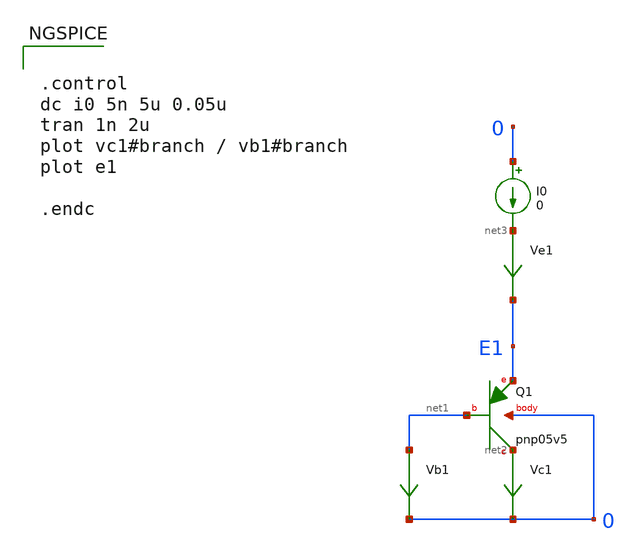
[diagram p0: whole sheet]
** sch_path: xyce/sky130A-xyce/libs.tech/xschem/sky130_tests/test_bipolar.sch
* Copyright 2020 Stefan Frederik Schippers
* Licensed under the Apache License, Version 2.0 (the "License");
* you may not use this file except in compliance with the License.
* You may obtain a copy of the License at
* https://www.apache.org/licenses/LICENSE-2.0
* Unless required by applicable law or agreed to in writing, software
* distributed under the License is distributed on an "AS IS" BASIS,
* WITHOUT WARRANTIES OR CONDITIONS OF ANY KIND, either express or implied.
* See the License for the specific language governing permissions and
* limitations under the License.
**.subckt test_bipolar
XQ1 net2 net1 E1 0 sky130_fd_pr__pnp_05v5_W0p68L0p68
Vc1 net2 0 0
.save i(vc1)
Vb1 net1 0 0
.save i(vb1)
I0 0 net3 0
Ve1 net3 E1 0
.save i(ve1)
**** begin user architecture code


.control
dc i0 5n 5u 0.05u
tran 1n 2u
plot vc1#branch / vb1#branch
plot e1

.endc



.include $::SKYWATER_MODELS/cells/nfet_01v8/sky130_fd_pr__nfet_01v8__tt.corner.spice
.include $::SKYWATER_MODELS/cells/nfet_01v8_lvt/sky130_fd_pr__nfet_01v8_lvt__tt.corner.spice
.include $::SKYWATER_MODELS/cells/pfet_01v8/sky130_fd_pr__pfet_01v8__tt.corner.spice
.include $::SKYWATER_MODELS/cells/nfet_03v3_nvt/sky130_fd_pr__nfet_03v3_nvt__tt.corner.spice
.include $::SKYWATER_MODELS/cells/nfet_05v0_nvt/sky130_fd_pr__nfet_05v0_nvt__tt.corner.spice
.include $::SKYWATER_MODELS/cells/esd_nfet_01v8/sky130_fd_pr__esd_nfet_01v8__tt.corner.spice
.include $::SKYWATER_MODELS/cells/pfet_01v8_lvt/sky130_fd_pr__pfet_01v8_lvt__tt.corner.spice
.include $::SKYWATER_MODELS/cells/pfet_01v8_hvt/sky130_fd_pr__pfet_01v8_hvt__tt.corner.spice
.include $::SKYWATER_MODELS/cells/esd_pfet_g5v0d10v5/sky130_fd_pr__esd_pfet_g5v0d10v5__tt.corner.spice
.include $::SKYWATER_MODELS/cells/pfet_g5v0d10v5/sky130_fd_pr__pfet_g5v0d10v5__tt.corner.spice
.include $::SKYWATER_MODELS/cells/pfet_g5v0d16v0/sky130_fd_pr__pfet_g5v0d16v0__tt.corner.spice
.include $::SKYWATER_MODELS/cells/nfet_g5v0d10v5/sky130_fd_pr__nfet_g5v0d10v5__tt.corner.spice
.include $::SKYWATER_MODELS/cells/nfet_g5v0d16v0/sky130_fd_pr__nfet_g5v0d16v0__tt_discrete.corner.spice
.include $::SKYWATER_MODELS/cells/esd_nfet_g5v0d10v5/sky130_fd_pr__esd_nfet_g5v0d10v5__tt.corner.spice
.include $::SKYWATER_MODELS/models/corners/tt/nonfet.spice
* Mismatch parameters
.include $::SKYWATER_MODELS/cells/nfet_01v8/sky130_fd_pr__nfet_01v8__mismatch.corner.spice
.include $::SKYWATER_MODELS/cells/pfet_01v8/sky130_fd_pr__pfet_01v8__mismatch.corner.spice
.include $::SKYWATER_MODELS/cells/nfet_01v8_lvt/sky130_fd_pr__nfet_01v8_lvt__mismatch.corner.spice
.include $::SKYWATER_MODELS/cells/pfet_01v8_lvt/sky130_fd_pr__pfet_01v8_lvt__mismatch.corner.spice
.include $::SKYWATER_MODELS/cells/pfet_01v8_hvt/sky130_fd_pr__pfet_01v8_hvt__mismatch.corner.spice
.include $::SKYWATER_MODELS/cells/nfet_g5v0d10v5/sky130_fd_pr__nfet_g5v0d10v5__mismatch.corner.spice
.include $::SKYWATER_MODELS/cells/pfet_g5v0d10v5/sky130_fd_pr__pfet_g5v0d10v5__mismatch.corner.spice
.include $::SKYWATER_MODELS/cells/nfet_05v0_nvt/sky130_fd_pr__nfet_05v0_nvt__mismatch.corner.spice
.include $::SKYWATER_MODELS/cells/nfet_03v3_nvt/sky130_fd_pr__nfet_03v3_nvt__mismatch.corner.spice
* Resistor$::SKYWATER_MODELS/Capacitor
.include $::SKYWATER_MODELS/models/r+c/res_typical__cap_typical.spice
.include $::SKYWATER_MODELS/models/r+c/res_typical__cap_typical__lin.spice
* Special cells
.include $::SKYWATER_MODELS/models/corners/tt/specialized_cells.spice
* All models
.include $::SKYWATER_MODELS/models/all.spice
* Corner
.include $::SKYWATER_MODELS/models/corners/tt/rf.spice

**** end user architecture code
**.ends
.end
